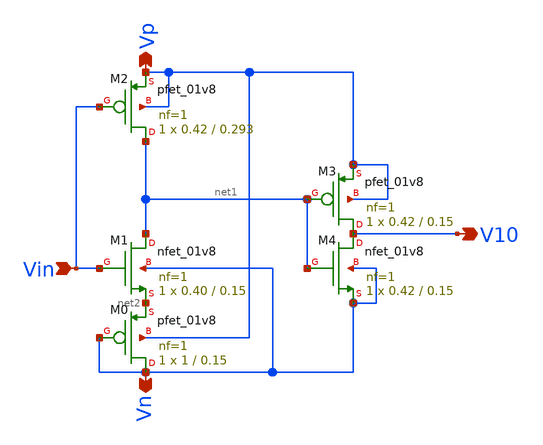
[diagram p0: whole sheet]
** sch_path: xschem/Vth_sch/Symbol/th10_backup.sch
**.subckt th10_backup Vn Vp Vin V10
*.opin Vn
*.opin Vp
*.ipin Vin
*.opin V10
XM3 V10 net1 Vp Vp sky130_fd_pr__pfet_01v8 L=0.15 W=0.42 nf=1 ad='int((nf+1)/2) * W/nf * 0.29' as='int((nf+2)/2) * W/nf * 0.29'
+ pd='2*int((nf+1)/2) * (W/nf + 0.29)' ps='2*int((nf+2)/2) * (W/nf + 0.29)' nrd='0.29 / W' nrs='0.29 / W'
+ sa=0 sb=0 sd=0 mult=1 m=1
XM4 V10 net1 Vn Vn sky130_fd_pr__nfet_01v8 L=0.15 W=0.42 nf=1 ad='int((nf+1)/2) * W/nf * 0.29' as='int((nf+2)/2) * W/nf * 0.29'
+ pd='2*int((nf+1)/2) * (W/nf + 0.29)' ps='2*int((nf+2)/2) * (W/nf + 0.29)' nrd='0.29 / W' nrs='0.29 / W'
+ sa=0 sb=0 sd=0 mult=1 m=1
XM2 net1 Vin Vp Vp sky130_fd_pr__pfet_01v8 L=0.293 W=0.42 nf=1 ad='int((nf+1)/2) * W/nf * 0.29' as='int((nf+2)/2) * W/nf * 0.29'
+ pd='2*int((nf+1)/2) * (W/nf + 0.29)' ps='2*int((nf+2)/2) * (W/nf + 0.29)' nrd='0.29 / W' nrs='0.29 / W'
+ sa=0 sb=0 sd=0 mult=1 m=1
XM1 net1 Vin net2 Vn sky130_fd_pr__nfet_01v8 L=0.15 W=0.40 nf=1 ad='int((nf+1)/2) * W/nf * 0.29' as='int((nf+2)/2) * W/nf * 0.29'
+ pd='2*int((nf+1)/2) * (W/nf + 0.29)' ps='2*int((nf+2)/2) * (W/nf + 0.29)' nrd='0.29 / W' nrs='0.29 / W'
+ sa=0 sb=0 sd=0 mult=1 m=1
XM0 Vn Vn net2 Vp sky130_fd_pr__pfet_01v8 L=0.15 W=1 nf=1 ad='int((nf+1)/2) * W/nf * 0.29' as='int((nf+2)/2) * W/nf * 0.29'
+ pd='2*int((nf+1)/2) * (W/nf + 0.29)' ps='2*int((nf+2)/2) * (W/nf + 0.29)' nrd='0.29 / W' nrs='0.29 / W'
+ sa=0 sb=0 sd=0 mult=1 m=1
**.ends
.end
